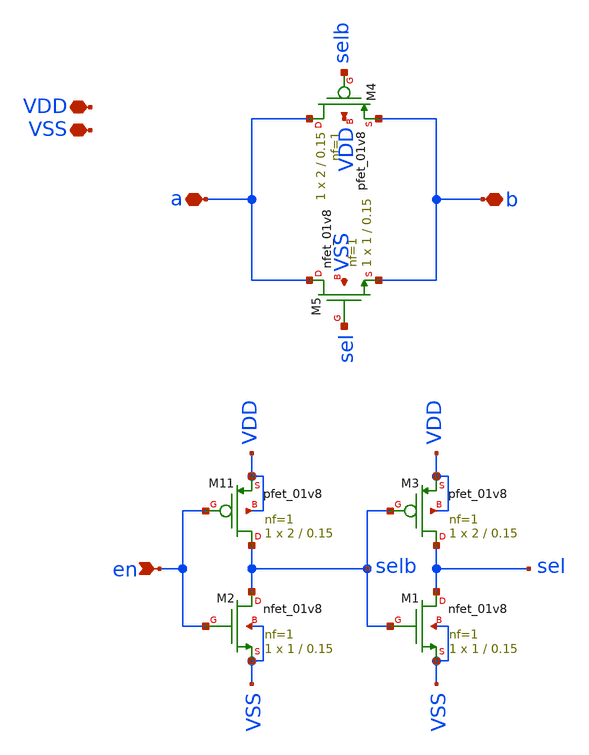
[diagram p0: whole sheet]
** sch_path: xsch/ip/tgate/tgate_6t.sch
**.subckt tgate_6t a b en VDD VSS
*.iopin a
*.iopin b
*.ipin en
*.iopin VDD
*.iopin VSS
XM2 selb en VSS VSS sky130_fd_pr__nfet_01v8 L=0.15 W=1 nf=1 ad='int((1 + 1)/2) * 1 / 1 * 0.29' as='int((1 + 2)/2) * 1 / 1 * 0.29'
+ pd='2*int((1 + 1)/2) * (1 / 1 + 0.29)' ps='2*int((1 + 2)/2) * (1 / 1 + 0.29)' nrd='0.29 / 1 ' nrs='0.29 / 1 '
+ sa=0 sb=0 sd=0 mult=1 m=1
XM11 selb en VDD VDD sky130_fd_pr__pfet_01v8 L=0.15 W=2 nf=1 ad='int((nf+1)/2) * W/nf * 0.29' as='int((nf+2)/2) * W/nf * 0.29'
+ pd='2*int((nf+1)/2) * (W/nf + 0.29)' ps='2*int((nf+2)/2) * (W/nf + 0.29)' nrd='0.29 / W' nrs='0.29 / W'
+ sa=0 sb=0 sd=0 mult=1 m=1
XM1 sel selb VSS VSS sky130_fd_pr__nfet_01v8 L=0.15 W=1 nf=1 ad='int((1 + 1)/2) * 1 / 1 * 0.29' as='int((1 + 2)/2) * 1 / 1 * 0.29'
+ pd='2*int((1 + 1)/2) * (1 / 1 + 0.29)' ps='2*int((1 + 2)/2) * (1 / 1 + 0.29)' nrd='0.29 / 1 ' nrs='0.29 / 1 '
+ sa=0 sb=0 sd=0 mult=1 m=1
XM3 sel selb VDD VDD sky130_fd_pr__pfet_01v8 L=0.15 W=2 nf=1 ad='int((nf+1)/2) * W/nf * 0.29' as='int((nf+2)/2) * W/nf * 0.29'
+ pd='2*int((nf+1)/2) * (W/nf + 0.29)' ps='2*int((nf+2)/2) * (W/nf + 0.29)' nrd='0.29 / W' nrs='0.29 / W'
+ sa=0 sb=0 sd=0 mult=1 m=1
XM4 a selb b VDD sky130_fd_pr__pfet_01v8 L=0.15 W=2 nf=1 ad='int((nf+1)/2) * W/nf * 0.29' as='int((nf+2)/2) * W/nf * 0.29'
+ pd='2*int((nf+1)/2) * (W/nf + 0.29)' ps='2*int((nf+2)/2) * (W/nf + 0.29)' nrd='0.29 / W' nrs='0.29 / W'
+ sa=0 sb=0 sd=0 mult=1 m=1
XM5 a sel b VSS sky130_fd_pr__nfet_01v8 L=0.15 W=1 nf=1 ad='int((1 + 1)/2) * 1 / 1 * 0.29' as='int((1 + 2)/2) * 1 / 1 * 0.29'
+ pd='2*int((1 + 1)/2) * (1 / 1 + 0.29)' ps='2*int((1 + 2)/2) * (1 / 1 + 0.29)' nrd='0.29 / 1 ' nrs='0.29 / 1 '
+ sa=0 sb=0 sd=0 mult=1 m=1
**.ends
.end
